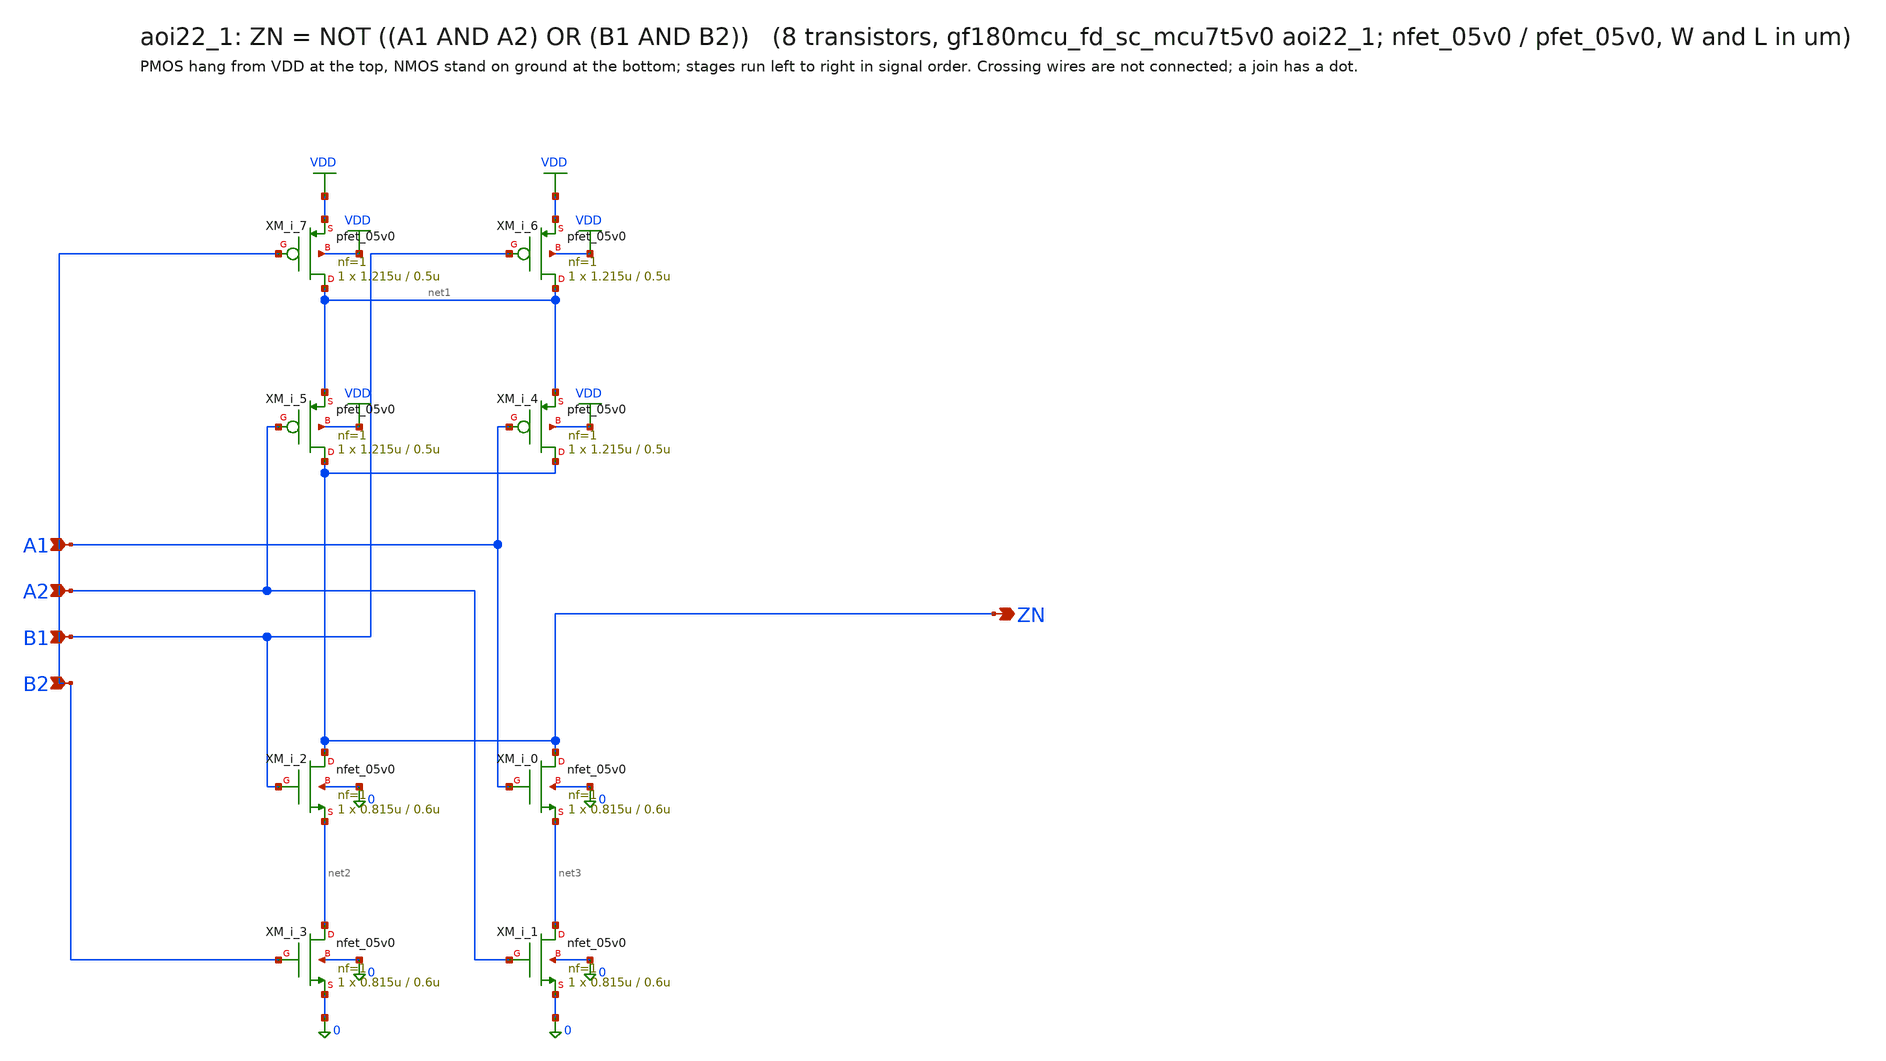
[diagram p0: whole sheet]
** sch_path: xschem/cells_tx/aoi22_1.sch
**.subckt aoi22_1 A1 A2 B1 B2 ZN
*.ipin A1
*.ipin A2
*.ipin B1
*.ipin B2
*.opin ZN
XM_i_3 net2 B2 0 0 nfet_05v0 L=0.6u W=0.815u nf=1 ad=4.075e-13 as=4.075e-13 pd=2.63e-06 ps=2.63e-06
+ nrd=0 nrs=0 sa=0 sb=0 sd=0 m=1
XM_i_2 ZN B1 net2 0 nfet_05v0 L=0.6u W=0.815u nf=1 ad=4.075e-13 as=4.075e-13 pd=2.63e-06 ps=2.63e-06
+ nrd=0 nrs=0 sa=0 sb=0 sd=0 m=1
XM_i_0 ZN A1 net3 0 nfet_05v0 L=0.6u W=0.815u nf=1 ad=4.075e-13 as=4.075e-13 pd=2.63e-06 ps=2.63e-06
+ nrd=0 nrs=0 sa=0 sb=0 sd=0 m=1
XM_i_1 net3 A2 0 0 nfet_05v0 L=0.6u W=0.815u nf=1 ad=4.075e-13 as=4.075e-13 pd=2.63e-06 ps=2.63e-06
+ nrd=0 nrs=0 sa=0 sb=0 sd=0 m=1
XM_i_7 net1 B2 VDD VDD pfet_05v0 L=0.5u W=1.215u nf=1 ad=6.075e-13 as=6.075e-13 pd=3.43e-06
+ ps=3.43e-06 nrd=0 nrs=0 sa=0 sb=0 sd=0 m=1
XM_i_6 net1 B1 VDD VDD pfet_05v0 L=0.5u W=1.215u nf=1 ad=6.075e-13 as=6.075e-13 pd=3.43e-06
+ ps=3.43e-06 nrd=0 nrs=0 sa=0 sb=0 sd=0 m=1
XM_i_4 ZN A1 net1 VDD pfet_05v0 L=0.5u W=1.215u nf=1 ad=6.075e-13 as=6.075e-13 pd=3.43e-06
+ ps=3.43e-06 nrd=0 nrs=0 sa=0 sb=0 sd=0 m=1
XM_i_5 ZN A2 net1 VDD pfet_05v0 L=0.5u W=1.215u nf=1 ad=6.075e-13 as=6.075e-13 pd=3.43e-06
+ ps=3.43e-06 nrd=0 nrs=0 sa=0 sb=0 sd=0 m=1
**.ends
.GLOBAL VDD
.end
